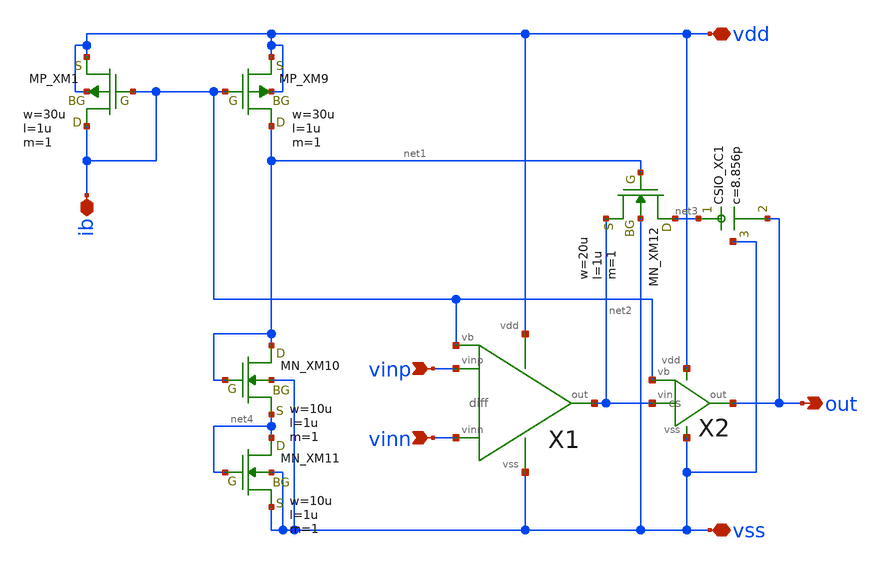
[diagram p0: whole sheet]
** sch_path: schematic/20250924_OSS_Workshop/ishikai/opamp/sample/opamp.sch
**.subckt opamp vinp vinn out vdd vss ib
*.ipin vinp
*.ipin vinn
*.opin out
*.iopin vdd
*.iopin vss
*.iopin ib
X1 vinp vinn net2 vdd vss ib diff
X2 net2 ib out vdd vss cs
XM9 net1 ib vdd vdd PMOS w=30u l=1u as=0 ad=0 ps=0 pd=0 nrd=0 nrs=0 m=1
XM12 net3 net1 net2 vss NMOS w=20u l=1u as=0 ad=0 ps=0 pd=0 nrd=0 nrs=0 m=1
XM1 ib ib vdd vdd PMOS w=30u l=1u as=0 ad=0 ps=0 pd=0 nrd=0 nrs=0 m=1
XM10 net1 net1 net4 vss NMOS w=10u l=1u as=0 ad=0 ps=0 pd=0 nrd=0 nrs=0 m=1
XM11 net4 net4 vss vss NMOS w=10u l=1u as=0 ad=0 ps=0 pd=0 nrd=0 nrs=0 m=1
XC1 net3 out vss F_CSIO c=8.856p x=120u y=120u m=1
**.ends

* expanding   symbol:  diff.sym # of pins=6
** sym_path: schematic/20250924_OSS_Workshop/ishikai/opamp/sample/diff.sym
** sch_path: schematic/20250924_OSS_Workshop/ishikai/opamp/sample/diff.sch
.subckt diff vinp vinn out vdd vss vb
*.ipin vinn
*.ipin vinp
*.ipin vb
*.opin out
*.iopin vdd
*.iopin vss
XM5 net2 vb vdd vdd PMOS w=180u l=1u as=0 ad=0 ps=0 pd=0 nrd=0 nrs=0 m=1
XM1 net1 vinn net2 net2 PMOS w=360u l=1u as=0 ad=0 ps=0 pd=0 nrd=0 nrs=0 m=1
XM2 out vinp net2 net2 PMOS w=360u l=1u as=0 ad=0 ps=0 pd=0 nrd=0 nrs=0 m=1
XM3 net1 net1 vss vss NMOS w=30u l=1u as=0 ad=0 ps=0 pd=0 nrd=0 nrs=0 m=1
XM4 out net1 vss vss NMOS w=30u l=1u as=0 ad=0 ps=0 pd=0 nrd=0 nrs=0 m=1
.ends


* expanding   symbol:  cs.sym # of pins=5
** sym_path: schematic/20250924_OSS_Workshop/ishikai/opamp/sample/cs.sym
** sch_path: schematic/20250924_OSS_Workshop/ishikai/opamp/sample/cs.sch
.subckt cs vin vb out vdd vss
*.ipin vb
*.ipin vin
*.opin out
*.iopin vss
*.iopin vdd
XM6 out vb vdd vdd PMOS w=270u l=1u as=0 ad=0 ps=0 pd=0 nrd=0 nrs=0 m=1
XM7 out vin vss vss NMOS w=90u l=1u as=0 ad=0 ps=0 pd=0 nrd=0 nrs=0 m=1
.ends

.end
